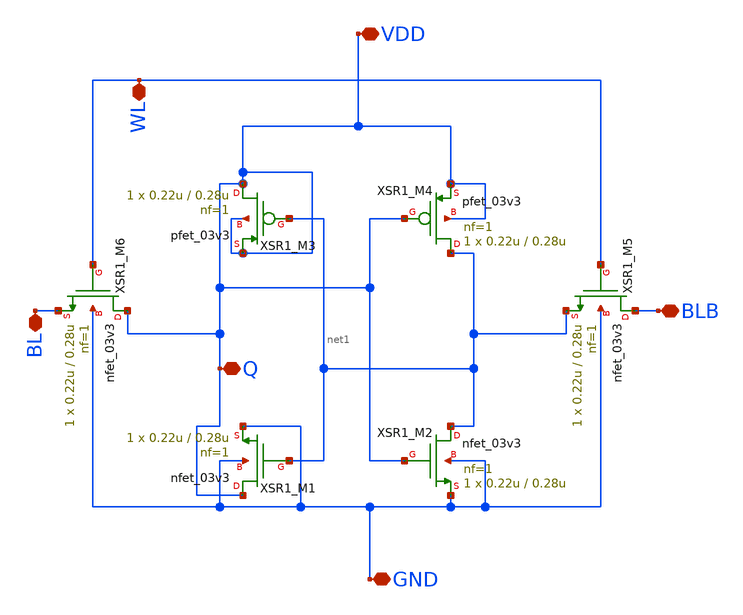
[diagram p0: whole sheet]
** sch_path: 6T4bit.sch
**.subckt 6T4bit BLB GND Q VDD BL WL
*.iopin BLB
*.iopin GND
*.iopin Q
*.iopin VDD
*.iopin BL
*.iopin WL
XSR1_M6 Q WL BL GND nfet_03v3 L=0.28u W=0.22u nf=1 ad='int((nf+1)/2) * W/nf * 0.18u' as='int((nf+2)/2) * W/nf * 0.18u'
+ pd='2*int((nf+1)/2) * (W/nf + 0.18u)' ps='2*int((nf+2)/2) * (W/nf + 0.18u)' nrd='0.18u / W' nrs='0.18u / W'
+ sa=0 sb=0 sd=0 m=1
XSR1_M3 Q net1 Q Q pfet_03v3 L=0.28u W=0.22u nf=1 ad='int((nf+1)/2) * W/nf * 0.18u' as='int((nf+2)/2) * W/nf * 0.18u'
+ pd='2*int((nf+1)/2) * (W/nf + 0.18u)' ps='2*int((nf+2)/2) * (W/nf + 0.18u)' nrd='0.18u / W' nrs='0.18u / W'
+ sa=0 sb=0 sd=0 m=1
XSR1_M4 net1 Q Q Q pfet_03v3 L=0.28u W=0.22u nf=1 ad='int((nf+1)/2) * W/nf * 0.18u' as='int((nf+2)/2) * W/nf * 0.18u'
+ pd='2*int((nf+1)/2) * (W/nf + 0.18u)' ps='2*int((nf+2)/2) * (W/nf + 0.18u)' nrd='0.18u / W' nrs='0.18u / W'
+ sa=0 sb=0 sd=0 m=1
XSR1_M5 BLB WL net1 GND nfet_03v3 L=0.28u W=0.22u nf=1 ad='int((nf+1)/2) * W/nf * 0.18u' as='int((nf+2)/2) * W/nf * 0.18u'
+ pd='2*int((nf+1)/2) * (W/nf + 0.18u)' ps='2*int((nf+2)/2) * (W/nf + 0.18u)' nrd='0.18u / W' nrs='0.18u / W'
+ sa=0 sb=0 sd=0 m=1
XSR1_M1 Q net1 GND GND nfet_03v3 L=0.28u W=0.22u nf=1 ad='int((nf+1)/2) * W/nf * 0.18u' as='int((nf+2)/2) * W/nf * 0.18u'
+ pd='2*int((nf+1)/2) * (W/nf + 0.18u)' ps='2*int((nf+2)/2) * (W/nf + 0.18u)' nrd='0.18u / W' nrs='0.18u / W'
+ sa=0 sb=0 sd=0 m=1
XSR1_M2 net1 Q GND GND nfet_03v3 L=0.28u W=0.22u nf=1 ad='int((nf+1)/2) * W/nf * 0.18u' as='int((nf+2)/2) * W/nf * 0.18u'
+ pd='2*int((nf+1)/2) * (W/nf + 0.18u)' ps='2*int((nf+2)/2) * (W/nf + 0.18u)' nrd='0.18u / W' nrs='0.18u / W'
+ sa=0 sb=0 sd=0 m=1
**.ends
.end
